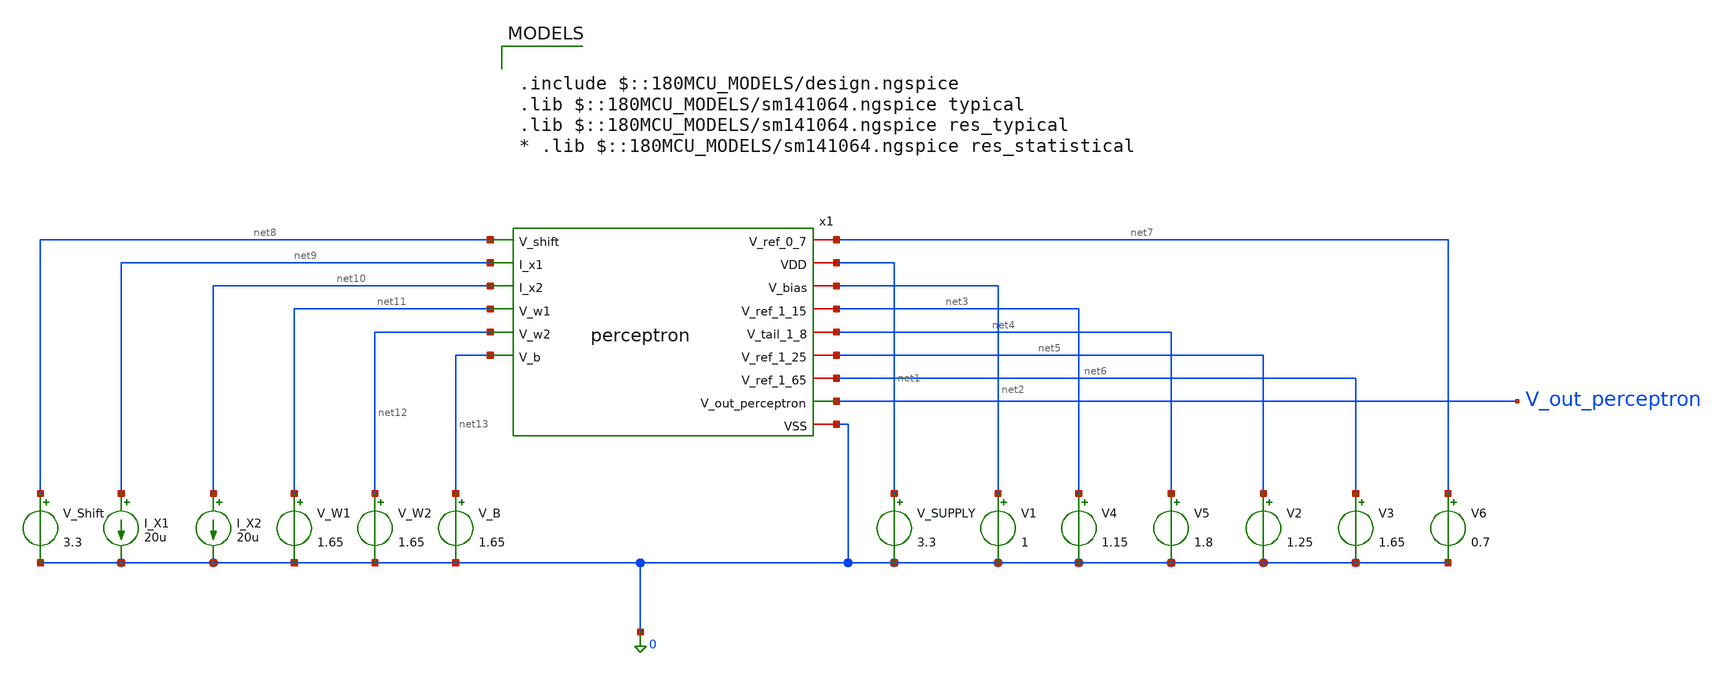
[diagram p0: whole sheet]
** sch_path: schematics/tb_perceptron.sch
**.subckt tb_perceptron
V_SUPPLY net1 0 3.3
V1 net2 0 1
V2 net5 0 1.25
V3 net6 0 1.65
V4 net3 0 1.15
V5 net4 0 1.8
V6 net7 0 0.7
I_X1 net9 0 20u
I_X2 net10 0 20u
V_W1 net11 0 1.65
V_W2 net12 0 1.65
V_B net13 0 1.65
V_Shift net8 0 3.3
x1 net7 net1 net2 net3 net4 net5 net6 net8 net9 net10 V_out_perceptron net11 net12 0 net13
+ perceptron
**** begin user architecture code


.control
  * --- start from neutral ---
  alter V_W1 = 1.65
  alter V_W2 = 1.65
  alter V_B  = 1.65
  alter I_X1 = 0
  alter I_X2 = 0

  * === Graph 1: Weight sweep (inhibitory / neutral / excitatory) ===
  alter I_X2 = 0
  alter V_W2 = 1.65
  alter V_B  = 1.65
  let n = 0
  dowhile n <= 2
    let vw1 = 1.45 + n * 0.2
    alter V_W1 = vw1
    dc I_X1 0 50u 1u
    wrdata /foss/designs/analog-perceptron-gf180mcu/plots/perceptron_graph1_weights.txt
+ v(V_out_perceptron)
    set appendwrite
    let n = n + 1
  end
  unset appendwrite
  alter V_W1 = 1.65

  * === Graph 2: Sensor 1 sweep, Sensor 2 interference ===
  alter V_W1 = 1.85
  alter V_W2 = 1.85
  alter V_B  = 1.65
  let n = 0
  dowhile n <= 2
    let ix2 = n * 25u
    alter I_X2 = ix2
    dc I_X1 0 50u 1u
    wrdata /foss/designs/analog-perceptron-gf180mcu/plots/perceptron_graph2_sensors.txt
+ v(V_out_perceptron)
    set appendwrite
    let n = n + 1
  end
  unset appendwrite
  alter V_W1 = 1.65
  alter V_W2 = 1.65
  alter I_X2 = 0

  * === Graph 3: Bias shifting ===
  alter I_X2 = 0
  alter V_W1 = 1.85
  let n = 0
  dowhile n <= 2
    let vb = 1.45 + n * 0.2
    alter V_B = vb
    dc I_X1 0 50u 1u
    wrdata /foss/designs/analog-perceptron-gf180mcu/plots/perceptron_graph3_bias.txt
+ v(V_out_perceptron)
    set appendwrite
    let n = n + 1
  end
  unset appendwrite
  alter V_W1 = 1.65
  alter V_B  = 1.65

  * === 3D Dataset A: I_X1 x I_X2 -> V_out ===
  alter V_W1 = 1.85
  alter V_W2 = 1.85
  alter V_B  = 1.65
  let n = 0
  dowhile n <= 25
    let ix2b = n * 2u
    alter I_X2 = ix2b
    dc I_X1 0 50u 1u
    wrdata /foss/designs/analog-perceptron-gf180mcu/plots/3d_sensors.txt v(V_out_perceptron)
    set appendwrite
    let n = n + 1
  end
  unset appendwrite
  alter V_W1 = 1.65
  alter V_W2 = 1.65
  alter I_X2 = 0

  * === 3D Dataset B: V_W1 x V_W2 -> V_out ===
  alter I_X1 = 50u
  alter I_X2 = 50u
  alter V_B  = 1.65
  let n = 0
  dowhile n <= 20
    let vw2 = 1.45 + n * 0.02
    alter V_W2 = vw2
    dc V_W1 1.45 1.85 0.01
    wrdata /foss/designs/analog-perceptron-gf180mcu/plots/3d_weights.txt v(V_out_perceptron)
    set appendwrite
    let n = n + 1
  end
  unset appendwrite

  * --- final state: neutral, zero input ---
  alter V_W1 = 1.65
  alter V_W2 = 1.65
  alter V_B  = 1.65
  alter I_X1 = 0
  alter I_X2 = 0
.endc



.include $::180MCU_MODELS/design.ngspice
.lib $::180MCU_MODELS/sm141064.ngspice typical
.lib $::180MCU_MODELS/sm141064.ngspice res_typical
* .lib $::180MCU_MODELS/sm141064.ngspice res_statistical

**** end user architecture code
**.ends

* expanding   symbol:  analog-perceptron-gf180mcu/schematics/perceptron.sym # of pins=15
** sym_path: schematics/perceptron.sym
** sch_path: schematics/perceptron.sch
.subckt perceptron V_ref_0_7 VDD V_bias V_ref_1_15 V_tail_1_8 V_ref_1_25 V_ref_1_65 V_shift I_x1
+ I_x2 V_out_perceptron V_w1 V_w2 VSS V_b
*.iopin VDD
*.iopin VSS
*.iopin V_bias
*.ipin I_x1
*.ipin I_x2
*.iopin V_ref_1_25
*.iopin V_ref_1_15
*.iopin V_ref_1_65
*.iopin V_tail_1_8
*.ipin V_w1
*.ipin V_w2
*.ipin V_b
*.iopin V_ref_0_7
*.opin V_out_perceptron
*.ipin V_shift
x1 V_ref_1_25 net4 V_bias I_x1 VSS cg_amp_tia
x2 V_ref_1_25 net3 V_bias I_x2 VSS cg_amp_tia
x_g1 net1 net2 V_w1 V_ref_1_65 V_ref_1_25 net4 V_tail_1_8 VSS gilbert_multiplier_current
x_g2 net1 net2 V_w2 V_ref_1_65 V_ref_1_25 net3 V_tail_1_8 VSS gilbert_multiplier_current
x_g3 net1 net2 V_b V_ref_1_65 V_ref_1_25 V_ref_1_15 V_tail_1_8 VSS gilbert_multiplier_current
x_tanh VDD V_ref_1_65 V_out_perceptron net1 net2 V_ref_0_7 VSS tanh_ota
XR1 net1 V_shift VSS ppolyf_u r_width=1e-6 r_length=7e-6 m=1
XR2 VDD net2 VSS ppolyf_u r_width=1e-6 r_length=7e-6 m=1
.ends


* expanding   symbol:  analog-perceptron-gf180mcu/schematics/cg_amp_tia.sym # of pins=5
** sym_path: schematics/cg_amp_tia.sym
** sch_path: schematics/cg_amp_tia.sch
.subckt cg_amp_tia V_ref V_out V_bias I_in VSS
*.iopin V_ref
*.iopin VSS
*.ipin I_in
*.ipin V_bias
*.opin V_out
XM1 V_out V_bias I_in VSS nfet_03v3 L=0.5u W=5u nf=1 ad='int((nf+1)/2) * W/nf * 0.18u' as='int((nf+2)/2) * W/nf * 0.18u'
+ pd='2*int((nf+1)/2) * (W/nf + 0.18u)' ps='2*int((nf+2)/2) * (W/nf + 0.18u)' nrd='0.18u / W' nrs='0.18u / W'
+ sa=0 sb=0 sd=0 m=1
XR1 V_out V_ref VSS ppolyf_u_1k r_width=3e-6 r_length=8.1e-6 m=1
.ends


* expanding   symbol:  analog-perceptron-gf180mcu/schematics/gilbert_multiplier_current.sym # of
*+ pins=8
** sym_path: schematics/gilbert_multiplier_current.sym
** sch_path: schematics/gilbert_multiplier_current.sch
.subckt gilbert_multiplier_current I_o_p I_o_n V_w_p V_w_n V_x_p V_x_n V_tail VSS
*.ipin V_x_p
*.ipin V_x_n
*.ipin V_tail
*.iopin VSS
*.ipin V_w_p
*.ipin V_w_n
*.opin I_o_n
*.opin I_o_p
XM1 net1 V_x_p net3 VSS nfet_03v3 L=0.5u W=10u nf=1 ad='int((nf+1)/2) * W/nf * 0.18u' as='int((nf+2)/2) * W/nf * 0.18u'
+ pd='2*int((nf+1)/2) * (W/nf + 0.18u)' ps='2*int((nf+2)/2) * (W/nf + 0.18u)' nrd='0.18u / W' nrs='0.18u / W'
+ sa=0 sb=0 sd=0 m=1
XM2 net2 V_x_n net4 VSS nfet_03v3 L=0.5u W=10u nf=1 ad='int((nf+1)/2) * W/nf * 0.18u' as='int((nf+2)/2) * W/nf * 0.18u'
+ pd='2*int((nf+1)/2) * (W/nf + 0.18u)' ps='2*int((nf+2)/2) * (W/nf + 0.18u)' nrd='0.18u / W' nrs='0.18u / W'
+ sa=0 sb=0 sd=0 m=1
XM3 I_o_n V_w_p net1 VSS nfet_03v3 L=0.5u W=10u nf=1 ad='int((nf+1)/2) * W/nf * 0.18u' as='int((nf+2)/2) * W/nf * 0.18u'
+ pd='2*int((nf+1)/2) * (W/nf + 0.18u)' ps='2*int((nf+2)/2) * (W/nf + 0.18u)' nrd='0.18u / W' nrs='0.18u / W'
+ sa=0 sb=0 sd=0 m=1
XM4 I_o_p V_w_n net1 VSS nfet_03v3 L=0.5u W=10u nf=1 ad='int((nf+1)/2) * W/nf * 0.18u' as='int((nf+2)/2) * W/nf * 0.18u'
+ pd='2*int((nf+1)/2) * (W/nf + 0.18u)' ps='2*int((nf+2)/2) * (W/nf + 0.18u)' nrd='0.18u / W' nrs='0.18u / W'
+ sa=0 sb=0 sd=0 m=1
XM5 I_o_n V_w_n net2 VSS nfet_03v3 L=0.5u W=10u nf=1 ad='int((nf+1)/2) * W/nf * 0.18u' as='int((nf+2)/2) * W/nf * 0.18u'
+ pd='2*int((nf+1)/2) * (W/nf + 0.18u)' ps='2*int((nf+2)/2) * (W/nf + 0.18u)' nrd='0.18u / W' nrs='0.18u / W'
+ sa=0 sb=0 sd=0 m=1
XM6 I_o_p V_w_p net2 VSS nfet_03v3 L=0.5u W=10u nf=1 ad='int((nf+1)/2) * W/nf * 0.18u' as='int((nf+2)/2) * W/nf * 0.18u'
+ pd='2*int((nf+1)/2) * (W/nf + 0.18u)' ps='2*int((nf+2)/2) * (W/nf + 0.18u)' nrd='0.18u / W' nrs='0.18u / W'
+ sa=0 sb=0 sd=0 m=1
XM7 net3 V_tail VSS VSS nfet_03v3 L=1u W=5u nf=1 ad='int((nf+1)/2) * W/nf * 0.18u' as='int((nf+2)/2) * W/nf * 0.18u'
+ pd='2*int((nf+1)/2) * (W/nf + 0.18u)' ps='2*int((nf+2)/2) * (W/nf + 0.18u)' nrd='0.18u / W' nrs='0.18u / W'
+ sa=0 sb=0 sd=0 m=1
XM8 net4 V_tail VSS VSS nfet_03v3 L=1u W=5u nf=1 ad='int((nf+1)/2) * W/nf * 0.18u' as='int((nf+2)/2) * W/nf * 0.18u'
+ pd='2*int((nf+1)/2) * (W/nf + 0.18u)' ps='2*int((nf+2)/2) * (W/nf + 0.18u)' nrd='0.18u / W' nrs='0.18u / W'
+ sa=0 sb=0 sd=0 m=1
XR1 net3 net4 VSS ppolyf_u_1k r_width=3e-6 r_length=46.2e-6 m=1
.ends


* expanding   symbol:  analog-perceptron-gf180mcu/schematics/tanh_ota.sym # of pins=7
** sym_path: schematics/tanh_ota.sym
** sch_path: schematics/tanh_ota.sch
.subckt tanh_ota VDD V_ref V_out V_in_p V_in_n V_bias VSS
*.iopin VDD
*.iopin VSS
*.ipin V_in_p
*.ipin V_in_n
*.ipin V_bias
*.opin V_out
*.iopin V_ref
XM1 net2 V_in_p net1 VSS nfet_03v3 L=0.5u W=10u nf=1 ad='int((nf+1)/2) * W/nf * 0.18u' as='int((nf+2)/2) * W/nf * 0.18u'
+ pd='2*int((nf+1)/2) * (W/nf + 0.18u)' ps='2*int((nf+2)/2) * (W/nf + 0.18u)' nrd='0.18u / W' nrs='0.18u / W'
+ sa=0 sb=0 sd=0 m=1
XM2 V_out V_in_n net1 VSS nfet_03v3 L=0.5u W=10u nf=1 ad='int((nf+1)/2) * W/nf * 0.18u' as='int((nf+2)/2) * W/nf * 0.18u'
+ pd='2*int((nf+1)/2) * (W/nf + 0.18u)' ps='2*int((nf+2)/2) * (W/nf + 0.18u)' nrd='0.18u / W' nrs='0.18u / W'
+ sa=0 sb=0 sd=0 m=1
XM3 net1 V_bias VSS VSS nfet_03v3 L=0.5u W=10u nf=1 ad='int((nf+1)/2) * W/nf * 0.18u' as='int((nf+2)/2) * W/nf * 0.18u'
+ pd='2*int((nf+1)/2) * (W/nf + 0.18u)' ps='2*int((nf+2)/2) * (W/nf + 0.18u)' nrd='0.18u / W' nrs='0.18u / W'
+ sa=0 sb=0 sd=0 m=1
XM4 net2 net2 VDD VDD pfet_03v3 L=0.5u W=20u nf=1 ad='int((nf+1)/2) * W/nf * 0.18u' as='int((nf+2)/2) * W/nf * 0.18u'
+ pd='2*int((nf+1)/2) * (W/nf + 0.18u)' ps='2*int((nf+2)/2) * (W/nf + 0.18u)' nrd='0.18u / W' nrs='0.18u / W'
+ sa=0 sb=0 sd=0 m=1
XM5 V_out net2 VDD VDD pfet_03v3 L=0.5u W=20u nf=1 ad='int((nf+1)/2) * W/nf * 0.18u' as='int((nf+2)/2) * W/nf * 0.18u'
+ pd='2*int((nf+1)/2) * (W/nf + 0.18u)' ps='2*int((nf+2)/2) * (W/nf + 0.18u)' nrd='0.18u / W' nrs='0.18u / W'
+ sa=0 sb=0 sd=0 m=1
XR1 net3 V_ref VSS ppolyf_u_1k r_width=3e-6 r_length=12.4e-6 m=1
XR2 net4 net3 VSS ppolyf_u_1k r_width=3e-6 r_length=12.4e-6 m=1
XR3 net5 net4 VSS ppolyf_u_1k r_width=3e-6 r_length=12.4e-6 m=1
XR4 net6 net5 VSS ppolyf_u_1k r_width=3e-6 r_length=12.4e-6 m=1
XR5 net7 net6 VSS ppolyf_u_1k r_width=3e-6 r_length=12.4e-6 m=1
XR6 V_out net7 VSS ppolyf_u_1k r_width=3e-6 r_length=12.4e-6 m=1
.ends

.end
